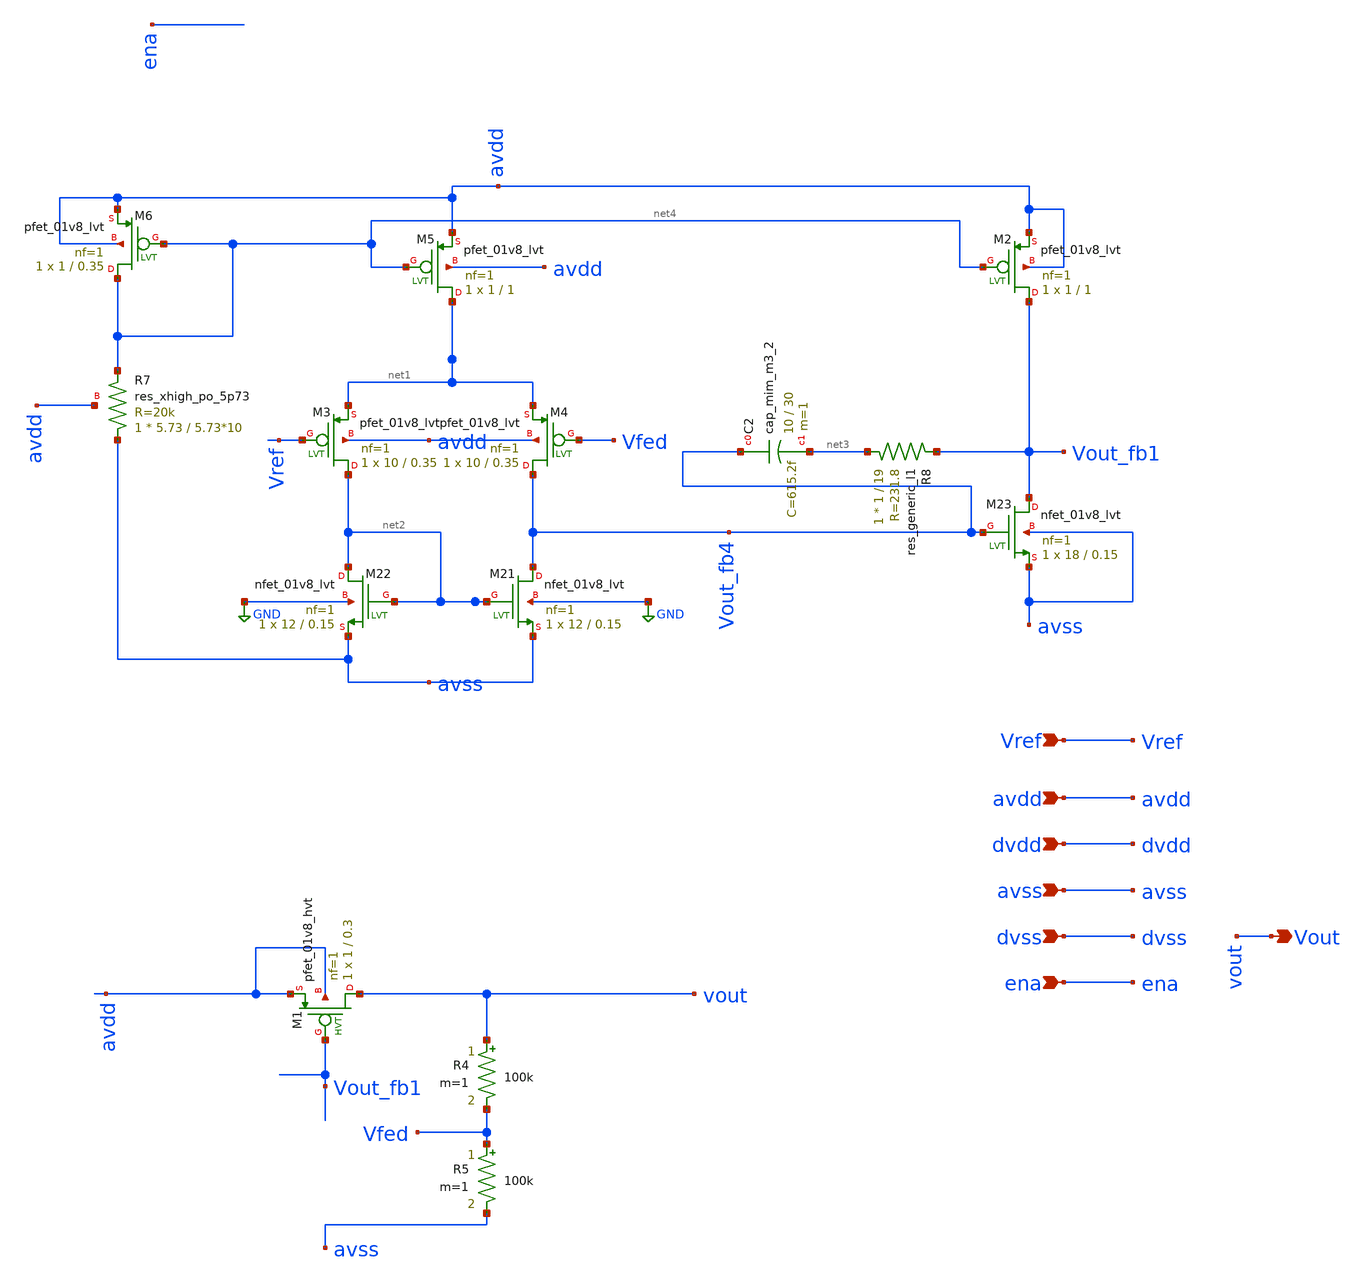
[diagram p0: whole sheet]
** sch_path: xschem/LDO_1.sch
**.subckt LDO_1 avdd dvss dvdd avss ena Vref Vout
*.ipin avdd
*.ipin dvss
*.ipin dvdd
*.ipin avss
*.ipin ena
*.ipin Vref
*.opin Vout
XM1 vout Vout_fb1 avdd avdd sky130_fd_pr__pfet_01v8_hvt L=0.3 W=1 nf=1 ad='int((nf+1)/2) * W/nf * 0.29'
+ as='int((nf+2)/2) * W/nf * 0.29' pd='2*int((nf+1)/2) * (W/nf + 0.29)' ps='2*int((nf+2)/2) * (W/nf + 0.29)'
+ nrd='0.29 / W' nrs='0.29 / W' sa=0 sb=0 sd=0 mult=1 m=1
R4 vout Vfed 100k m=1
R5 Vfed avss 100k m=1
XM21 Vout_fb4 net2 avss GND sky130_fd_pr__nfet_01v8_lvt L=0.15 W=12 nf=1 ad='int((nf+1)/2) * W/nf * 0.29'
+ as='int((nf+2)/2) * W/nf * 0.29' pd='2*int((nf+1)/2) * (W/nf + 0.29)' ps='2*int((nf+2)/2) * (W/nf + 0.29)'
+ nrd='0.29 / W' nrs='0.29 / W' sa=0 sb=0 sd=0 mult=1 m=1
XM22 net2 net2 avss GND sky130_fd_pr__nfet_01v8_lvt L=0.15 W=12 nf=1 ad='int((nf+1)/2) * W/nf * 0.29'
+ as='int((nf+2)/2) * W/nf * 0.29' pd='2*int((nf+1)/2) * (W/nf + 0.29)' ps='2*int((nf+2)/2) * (W/nf + 0.29)'
+ nrd='0.29 / W' nrs='0.29 / W' sa=0 sb=0 sd=0 mult=1 m=1
XM23 Vout_fb1 Vout_fb4 avss avss sky130_fd_pr__nfet_01v8_lvt L=0.15 W=18 nf=1 ad='int((nf+1)/2) * W/nf * 0.29'
+ as='int((nf+2)/2) * W/nf * 0.29' pd='2*int((nf+1)/2) * (W/nf + 0.29)' ps='2*int((nf+2)/2) * (W/nf + 0.29)'
+ nrd='0.29 / W' nrs='0.29 / W' sa=0 sb=0 sd=0 mult=1 m=1
XM2 Vout_fb1 net4 avdd avdd sky130_fd_pr__pfet_01v8_lvt L=1 W=1 nf=1 ad='int((nf+1)/2) * W/nf * 0.29'
+ as='int((nf+2)/2) * W/nf * 0.29' pd='2*int((nf+1)/2) * (W/nf + 0.29)' ps='2*int((nf+2)/2) * (W/nf + 0.29)'
+ nrd='0.29 / W' nrs='0.29 / W' sa=0 sb=0 sd=0 mult=1 m=1
XM3 net2 Vref net1 avdd sky130_fd_pr__pfet_01v8_lvt L=0.35 W=10 nf=1 ad='int((nf+1)/2) * W/nf * 0.29'
+ as='int((nf+2)/2) * W/nf * 0.29' pd='2*int((nf+1)/2) * (W/nf + 0.29)' ps='2*int((nf+2)/2) * (W/nf + 0.29)'
+ nrd='0.29 / W' nrs='0.29 / W' sa=0 sb=0 sd=0 mult=1 m=1
XM4 Vout_fb4 Vfed net1 avdd sky130_fd_pr__pfet_01v8_lvt L=0.35 W=10 nf=1 ad='int((nf+1)/2) * W/nf * 0.29'
+ as='int((nf+2)/2) * W/nf * 0.29' pd='2*int((nf+1)/2) * (W/nf + 0.29)' ps='2*int((nf+2)/2) * (W/nf + 0.29)'
+ nrd='0.29 / W' nrs='0.29 / W' sa=0 sb=0 sd=0 mult=1 m=1
XM5 net1 net4 avdd avdd sky130_fd_pr__pfet_01v8_lvt L=1 W=1 nf=1 ad='int((nf+1)/2) * W/nf * 0.29' as='int((nf+2)/2) * W/nf * 0.29'
+ pd='2*int((nf+1)/2) * (W/nf + 0.29)' ps='2*int((nf+2)/2) * (W/nf + 0.29)' nrd='0.29 / W' nrs='0.29 / W'
+ sa=0 sb=0 sd=0 mult=1 m=1
XM6 net4 net4 avdd avdd sky130_fd_pr__pfet_01v8_lvt L=0.35 W=1 nf=1 ad='int((nf+1)/2) * W/nf * 0.29'
+ as='int((nf+2)/2) * W/nf * 0.29' pd='2*int((nf+1)/2) * (W/nf + 0.29)' ps='2*int((nf+2)/2) * (W/nf + 0.29)'
+ nrd='0.29 / W' nrs='0.29 / W' sa=0 sb=0 sd=0 mult=1 m=1
XR7 avss net4 avdd sky130_fd_pr__res_xhigh_po_5p73 L=5.73*10 mult=1 m=1
XC2 Vout_fb4 net3 sky130_fd_pr__cap_mim_m3_2 W=10 L=30 MF=1 m=1
R8 net3 Vout_fb1 sky130_fd_pr__res_generic_l1 W=1 L=19 m=1
**.ends
.GLOBAL GND
.end
